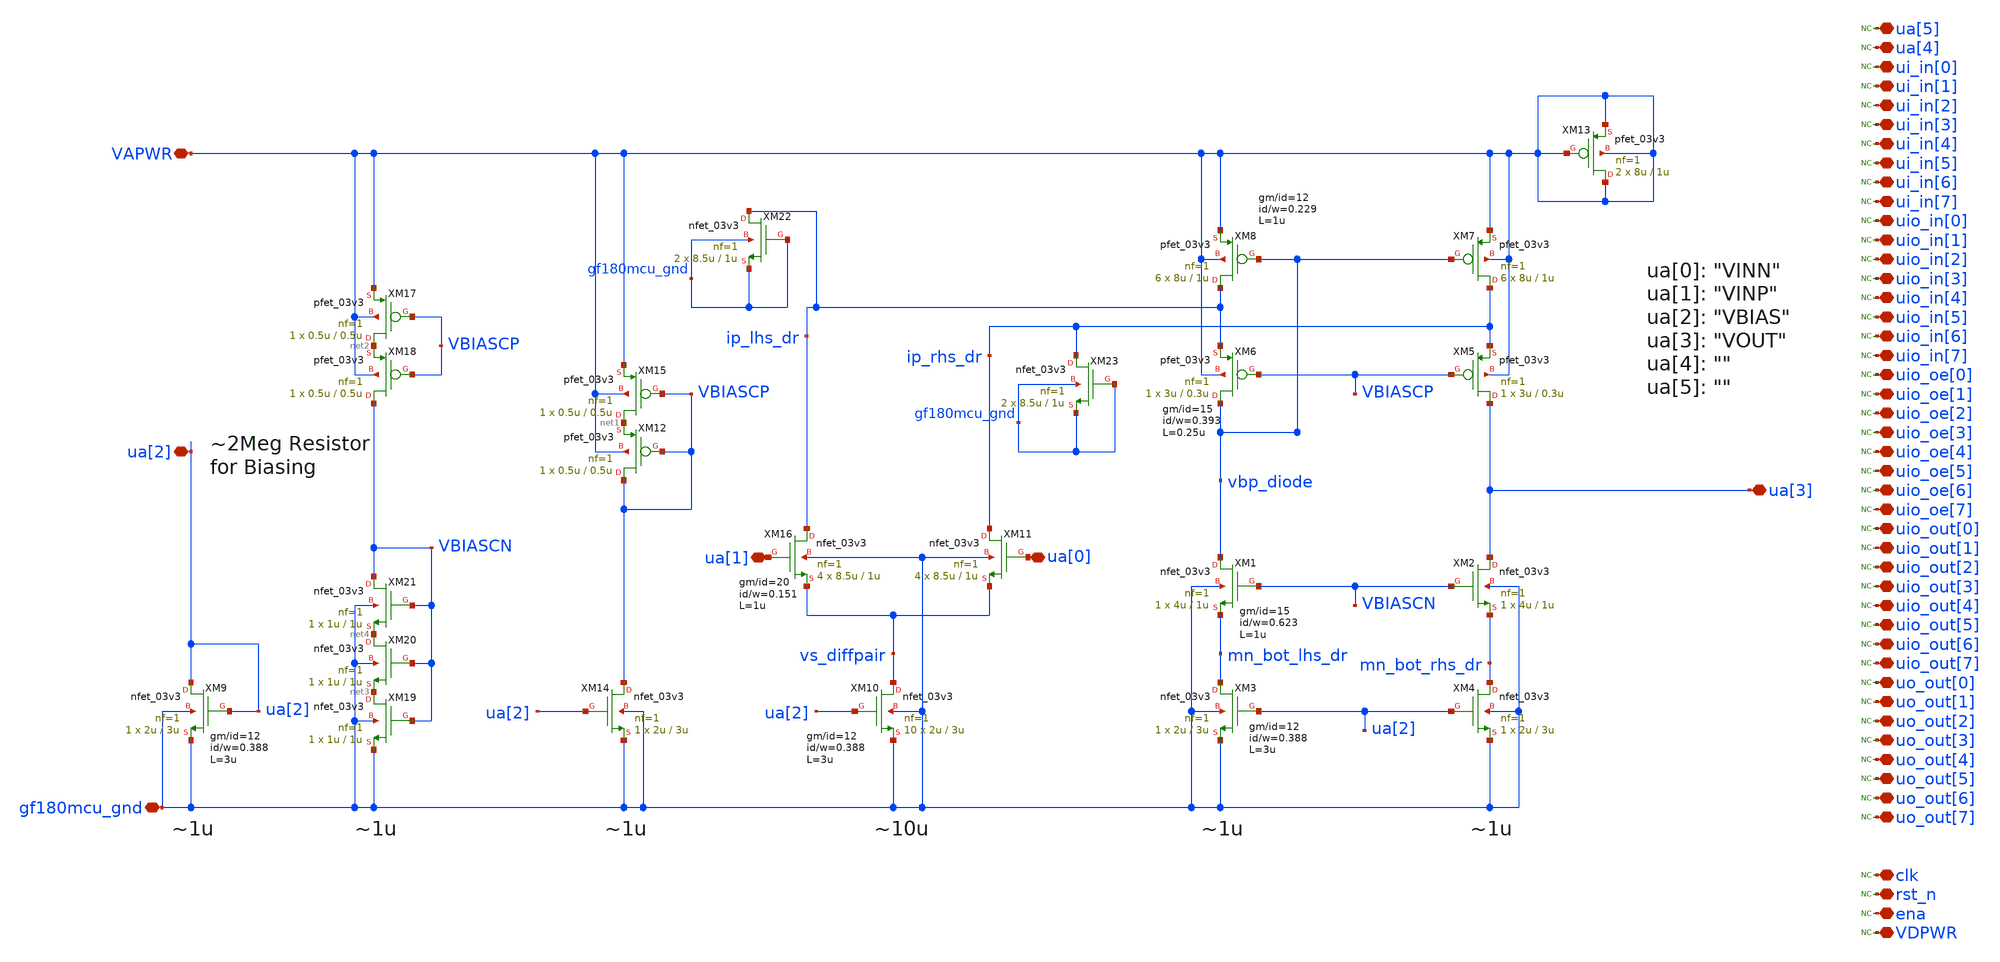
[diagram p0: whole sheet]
** sch_path: SCH/XSCHEM_SCH/TTGF0P3_LPCAS_FC_OTA.sch
**.subckt TTGF0P3_LPCAS_FC_OTA ua[3] ua[1] ua[0] VAPWR ua[2] gf180mcu_gnd ui_in[4] ui_in[5] ui_in[6]
*+ ui_in[7] uio_in[0] uio_in[1] uio_in[2] uio_in[3] uio_in[4] uio_in[5] uio_in[6] uio_in[7] uio_oe[0] uio_oe[1]
*+ uio_oe[2] uio_oe[3] uio_oe[4] uio_oe[5] uio_oe[6] uio_oe[7] uio_out[0] uio_out[1] uio_out[2] uio_out[3]
*+ uio_out[4] uio_out[5] uio_out[6] uio_out[7] uo_out[0] uo_out[1] uo_out[2] uo_out[3] uo_out[4] uo_out[5]
*+ uo_out[6] uo_out[7] clk rst_n ena ua[4] ua[5] ui_in[0] ui_in[3] ui_in[1] ui_in[2] VDPWR
*.iopin ua[3]
*.iopin ua[1]
*.iopin ua[0]
*.iopin VAPWR
*.iopin ua[2]
*.iopin gf180mcu_gnd
*.iopin ui_in[4]
*.iopin ui_in[5]
*.iopin ui_in[6]
*.iopin ui_in[7]
*.iopin uio_in[0]
*.iopin uio_in[1]
*.iopin uio_in[2]
*.iopin uio_in[3]
*.iopin uio_in[4]
*.iopin uio_in[5]
*.iopin uio_in[6]
*.iopin uio_in[7]
*.iopin uio_oe[0]
*.iopin uio_oe[1]
*.iopin uio_oe[2]
*.iopin uio_oe[3]
*.iopin uio_oe[4]
*.iopin uio_oe[5]
*.iopin uio_oe[6]
*.iopin uio_oe[7]
*.iopin uio_out[0]
*.iopin uio_out[1]
*.iopin uio_out[2]
*.iopin uio_out[3]
*.iopin uio_out[4]
*.iopin uio_out[5]
*.iopin uio_out[6]
*.iopin uio_out[7]
*.iopin uo_out[0]
*.iopin uo_out[1]
*.iopin uo_out[2]
*.iopin uo_out[3]
*.iopin uo_out[4]
*.iopin uo_out[5]
*.iopin uo_out[6]
*.iopin uo_out[7]
*.iopin clk
*.iopin rst_n
*.iopin ena
*.iopin ua[4]
*.iopin ua[5]
*.iopin ui_in[0]
*.iopin ui_in[3]
*.iopin ui_in[1]
*.iopin ui_in[2]
*.iopin VDPWR
XM1 vbp_diode VBIASCN mn_bot_lhs_dr gf180mcu_gnd nfet_03v3 L=1u W=4u nf=1 ad='int((nf+1)/2) * W/nf * 0.18u'
+ as='int((nf+2)/2) * W/nf * 0.18u' pd='2*int((nf+1)/2) * (W/nf + 0.18u)' ps='2*int((nf+2)/2) * (W/nf + 0.18u)'
+ nrd='0.18u / W' nrs='0.18u / W' sa=0 sb=0 sd=0 m=1
XM2 ua[3] VBIASCN mn_bot_rhs_dr gf180mcu_gnd nfet_03v3 L=1u W=4u nf=1 ad='int((nf+1)/2) * W/nf * 0.18u'
+ as='int((nf+2)/2) * W/nf * 0.18u' pd='2*int((nf+1)/2) * (W/nf + 0.18u)' ps='2*int((nf+2)/2) * (W/nf + 0.18u)'
+ nrd='0.18u / W' nrs='0.18u / W' sa=0 sb=0 sd=0 m=1
XM5 ua[3] VBIASCP ip_rhs_dr VAPWR pfet_03v3 L=0.3u W=3u nf=1 ad='int((nf+1)/2) * W/nf * 0.18u' as='int((nf+2)/2) * W/nf * 0.18u'
+ pd='2*int((nf+1)/2) * (W/nf + 0.18u)' ps='2*int((nf+2)/2) * (W/nf + 0.18u)' nrd='0.18u / W' nrs='0.18u / W'
+ sa=0 sb=0 sd=0 m=1
XM6 vbp_diode VBIASCP ip_lhs_dr VAPWR pfet_03v3 L=0.3u W=3u nf=1 ad='int((nf+1)/2) * W/nf * 0.18u' as='int((nf+2)/2) * W/nf * 0.18u'
+ pd='2*int((nf+1)/2) * (W/nf + 0.18u)' ps='2*int((nf+2)/2) * (W/nf + 0.18u)' nrd='0.18u / W' nrs='0.18u / W'
+ sa=0 sb=0 sd=0 m=1
XM7 ip_rhs_dr vbp_diode VAPWR VAPWR pfet_03v3 L=1u W=8u nf=1 ad='int((nf+1)/2) * W/nf * 0.18u' as='int((nf+2)/2) * W/nf * 0.18u'
+ pd='2*int((nf+1)/2) * (W/nf + 0.18u)' ps='2*int((nf+2)/2) * (W/nf + 0.18u)' nrd='0.18u / W' nrs='0.18u / W'
+ sa=0 sb=0 sd=0 m=6
XM8 ip_lhs_dr vbp_diode VAPWR VAPWR pfet_03v3 L=1u W=8u nf=1 ad='int((nf+1)/2) * W/nf * 0.18u' as='int((nf+2)/2) * W/nf * 0.18u'
+ pd='2*int((nf+1)/2) * (W/nf + 0.18u)' ps='2*int((nf+2)/2) * (W/nf + 0.18u)' nrd='0.18u / W' nrs='0.18u / W'
+ sa=0 sb=0 sd=0 m=6
XM9 ua[2] ua[2] gf180mcu_gnd gf180mcu_gnd nfet_03v3 L=3u W=2u nf=1 ad='int((nf+1)/2) * W/nf * 0.18u'
+ as='int((nf+2)/2) * W/nf * 0.18u' pd='2*int((nf+1)/2) * (W/nf + 0.18u)' ps='2*int((nf+2)/2) * (W/nf + 0.18u)'
+ nrd='0.18u / W' nrs='0.18u / W' sa=0 sb=0 sd=0 m=1
XM10 vs_diffpair ua[2] gf180mcu_gnd gf180mcu_gnd nfet_03v3 L=3u W=2u nf=1 ad='int((nf+1)/2) * W/nf * 0.18u'
+ as='int((nf+2)/2) * W/nf * 0.18u' pd='2*int((nf+1)/2) * (W/nf + 0.18u)' ps='2*int((nf+2)/2) * (W/nf + 0.18u)'
+ nrd='0.18u / W' nrs='0.18u / W' sa=0 sb=0 sd=0 m=10
XM3 mn_bot_lhs_dr ua[2] gf180mcu_gnd gf180mcu_gnd nfet_03v3 L=3u W=2u nf=1 ad='int((nf+1)/2) * W/nf * 0.18u'
+ as='int((nf+2)/2) * W/nf * 0.18u' pd='2*int((nf+1)/2) * (W/nf + 0.18u)' ps='2*int((nf+2)/2) * (W/nf + 0.18u)'
+ nrd='0.18u / W' nrs='0.18u / W' sa=0 sb=0 sd=0 m=1
XM4 mn_bot_rhs_dr ua[2] gf180mcu_gnd gf180mcu_gnd nfet_03v3 L=3u W=2u nf=1 ad='int((nf+1)/2) * W/nf * 0.18u'
+ as='int((nf+2)/2) * W/nf * 0.18u' pd='2*int((nf+1)/2) * (W/nf + 0.18u)' ps='2*int((nf+2)/2) * (W/nf + 0.18u)'
+ nrd='0.18u / W' nrs='0.18u / W' sa=0 sb=0 sd=0 m=1
XM14 VBIASCP ua[2] gf180mcu_gnd gf180mcu_gnd nfet_03v3 L=3u W=2u nf=1 ad='int((nf+1)/2) * W/nf * 0.18u'
+ as='int((nf+2)/2) * W/nf * 0.18u' pd='2*int((nf+1)/2) * (W/nf + 0.18u)' ps='2*int((nf+2)/2) * (W/nf + 0.18u)'
+ nrd='0.18u / W' nrs='0.18u / W' sa=0 sb=0 sd=0 m=1
XM15 net1 VBIASCP VAPWR VAPWR pfet_03v3 L=0.5u W=0.5u nf=1 ad='int((nf+1)/2) * W/nf * 0.18u' as='int((nf+2)/2) * W/nf * 0.18u'
+ pd='2*int((nf+1)/2) * (W/nf + 0.18u)' ps='2*int((nf+2)/2) * (W/nf + 0.18u)' nrd='0.18u / W' nrs='0.18u / W'
+ sa=0 sb=0 sd=0 m=1
XM16 ip_lhs_dr ua[1] vs_diffpair gf180mcu_gnd nfet_03v3 L=1u W=8.5u nf=1 ad='int((nf+1)/2) * W/nf * 0.18u'
+ as='int((nf+2)/2) * W/nf * 0.18u' pd='2*int((nf+1)/2) * (W/nf + 0.18u)' ps='2*int((nf+2)/2) * (W/nf + 0.18u)'
+ nrd='0.18u / W' nrs='0.18u / W' sa=0 sb=0 sd=0 m=4
XM11 ip_rhs_dr ua[0] vs_diffpair gf180mcu_gnd nfet_03v3 L=1u W=8.5u nf=1 ad='int((nf+1)/2) * W/nf * 0.18u'
+ as='int((nf+2)/2) * W/nf * 0.18u' pd='2*int((nf+1)/2) * (W/nf + 0.18u)' ps='2*int((nf+2)/2) * (W/nf + 0.18u)'
+ nrd='0.18u / W' nrs='0.18u / W' sa=0 sb=0 sd=0 m=4
XM12 VBIASCP VBIASCP net1 VAPWR pfet_03v3 L=0.5u W=0.5u nf=1 ad='int((nf+1)/2) * W/nf * 0.18u' as='int((nf+2)/2) * W/nf * 0.18u'
+ pd='2*int((nf+1)/2) * (W/nf + 0.18u)' ps='2*int((nf+2)/2) * (W/nf + 0.18u)' nrd='0.18u / W' nrs='0.18u / W'
+ sa=0 sb=0 sd=0 m=1
XM17 net2 VBIASCP VAPWR VAPWR pfet_03v3 L=0.5u W=0.5u nf=1 ad='int((nf+1)/2) * W/nf * 0.18u' as='int((nf+2)/2) * W/nf * 0.18u'
+ pd='2*int((nf+1)/2) * (W/nf + 0.18u)' ps='2*int((nf+2)/2) * (W/nf + 0.18u)' nrd='0.18u / W' nrs='0.18u / W'
+ sa=0 sb=0 sd=0 m=1
XM18 VBIASCN VBIASCP net2 VAPWR pfet_03v3 L=0.5u W=0.5u nf=1 ad='int((nf+1)/2) * W/nf * 0.18u' as='int((nf+2)/2) * W/nf * 0.18u'
+ pd='2*int((nf+1)/2) * (W/nf + 0.18u)' ps='2*int((nf+2)/2) * (W/nf + 0.18u)' nrd='0.18u / W' nrs='0.18u / W'
+ sa=0 sb=0 sd=0 m=1
XM19 net3 VBIASCN gf180mcu_gnd gf180mcu_gnd nfet_03v3 L=1u W=1u nf=1 ad='int((nf+1)/2) * W/nf * 0.18u'
+ as='int((nf+2)/2) * W/nf * 0.18u' pd='2*int((nf+1)/2) * (W/nf + 0.18u)' ps='2*int((nf+2)/2) * (W/nf + 0.18u)'
+ nrd='0.18u / W' nrs='0.18u / W' sa=0 sb=0 sd=0 m=1
XM20 net4 VBIASCN net3 gf180mcu_gnd nfet_03v3 L=1u W=1u nf=1 ad='int((nf+1)/2) * W/nf * 0.18u' as='int((nf+2)/2) * W/nf * 0.18u'
+ pd='2*int((nf+1)/2) * (W/nf + 0.18u)' ps='2*int((nf+2)/2) * (W/nf + 0.18u)' nrd='0.18u / W' nrs='0.18u / W'
+ sa=0 sb=0 sd=0 m=1
XM21 VBIASCN VBIASCN net4 gf180mcu_gnd nfet_03v3 L=1u W=1u nf=1 ad='int((nf+1)/2) * W/nf * 0.18u' as='int((nf+2)/2) * W/nf * 0.18u'
+ pd='2*int((nf+1)/2) * (W/nf + 0.18u)' ps='2*int((nf+2)/2) * (W/nf + 0.18u)' nrd='0.18u / W' nrs='0.18u / W'
+ sa=0 sb=0 sd=0 m=1
* noconn ua[5]
* noconn ua[4]
* noconn ui_in[0]
* noconn ui_in[1]
* noconn ui_in[2]
* noconn ui_in[3]
* noconn ui_in[4]
* noconn ui_in[5]
* noconn ui_in[6]
* noconn ui_in[7]
* noconn uio_in[0]
* noconn uio_in[1]
* noconn uio_in[2]
* noconn uio_in[3]
* noconn uio_in[4]
* noconn uio_in[5]
* noconn uio_in[6]
* noconn uio_in[7]
* noconn uio_oe[0]
* noconn uio_oe[1]
* noconn uio_oe[2]
* noconn uio_oe[3]
* noconn uio_oe[4]
* noconn uio_oe[5]
* noconn uio_oe[6]
* noconn uio_oe[7]
* noconn uio_out[0]
* noconn uio_out[1]
* noconn uio_out[2]
* noconn uio_out[3]
* noconn uio_out[4]
* noconn uio_out[5]
* noconn uio_out[6]
* noconn uio_out[7]
* noconn uo_out[0]
* noconn uo_out[1]
* noconn uo_out[2]
* noconn uo_out[3]
* noconn uo_out[4]
* noconn uo_out[5]
* noconn uo_out[6]
* noconn uo_out[7]
* noconn clk
* noconn rst_n
* noconn ena
* noconn VDPWR
XM13 VAPWR VAPWR VAPWR VAPWR pfet_03v3 L=1u W=8u nf=1 ad='int((nf+1)/2) * W/nf * 0.18u' as='int((nf+2)/2) * W/nf * 0.18u'
+ pd='2*int((nf+1)/2) * (W/nf + 0.18u)' ps='2*int((nf+2)/2) * (W/nf + 0.18u)' nrd='0.18u / W' nrs='0.18u / W'
+ sa=0 sb=0 sd=0 m=2
XM22 ip_lhs_dr gf180mcu_gnd gf180mcu_gnd gf180mcu_gnd nfet_03v3 L=1u W=8.5u nf=1 ad='int((nf+1)/2) * W/nf * 0.18u'
+ as='int((nf+2)/2) * W/nf * 0.18u' pd='2*int((nf+1)/2) * (W/nf + 0.18u)' ps='2*int((nf+2)/2) * (W/nf + 0.18u)'
+ nrd='0.18u / W' nrs='0.18u / W' sa=0 sb=0 sd=0 m=2
XM23 ip_rhs_dr gf180mcu_gnd gf180mcu_gnd gf180mcu_gnd nfet_03v3 L=1u W=8.5u nf=1 ad='int((nf+1)/2) * W/nf * 0.18u'
+ as='int((nf+2)/2) * W/nf * 0.18u' pd='2*int((nf+1)/2) * (W/nf + 0.18u)' ps='2*int((nf+2)/2) * (W/nf + 0.18u)'
+ nrd='0.18u / W' nrs='0.18u / W' sa=0 sb=0 sd=0 m=2
**.ends
.end
